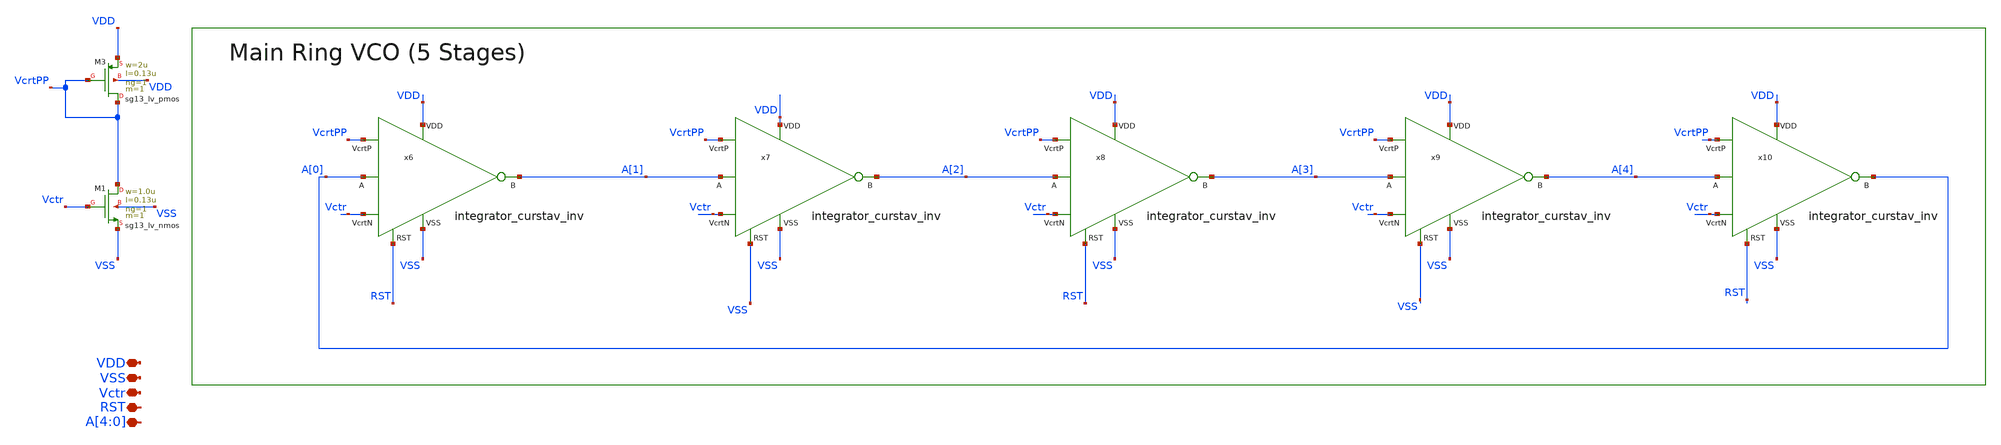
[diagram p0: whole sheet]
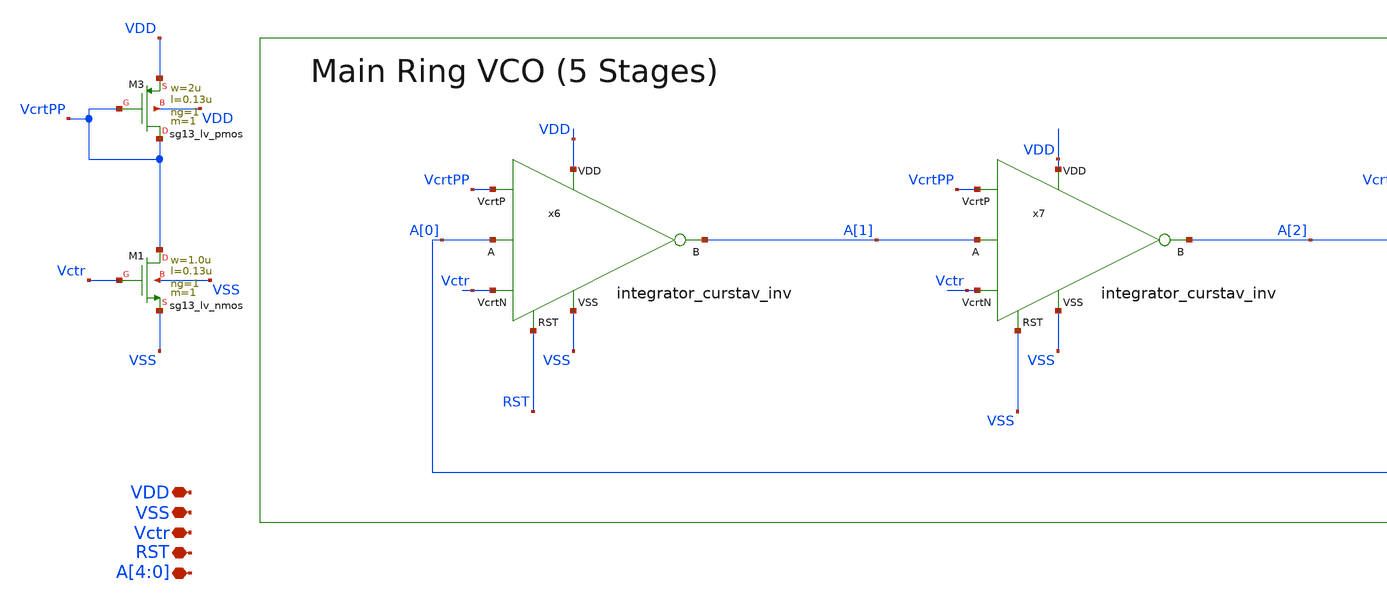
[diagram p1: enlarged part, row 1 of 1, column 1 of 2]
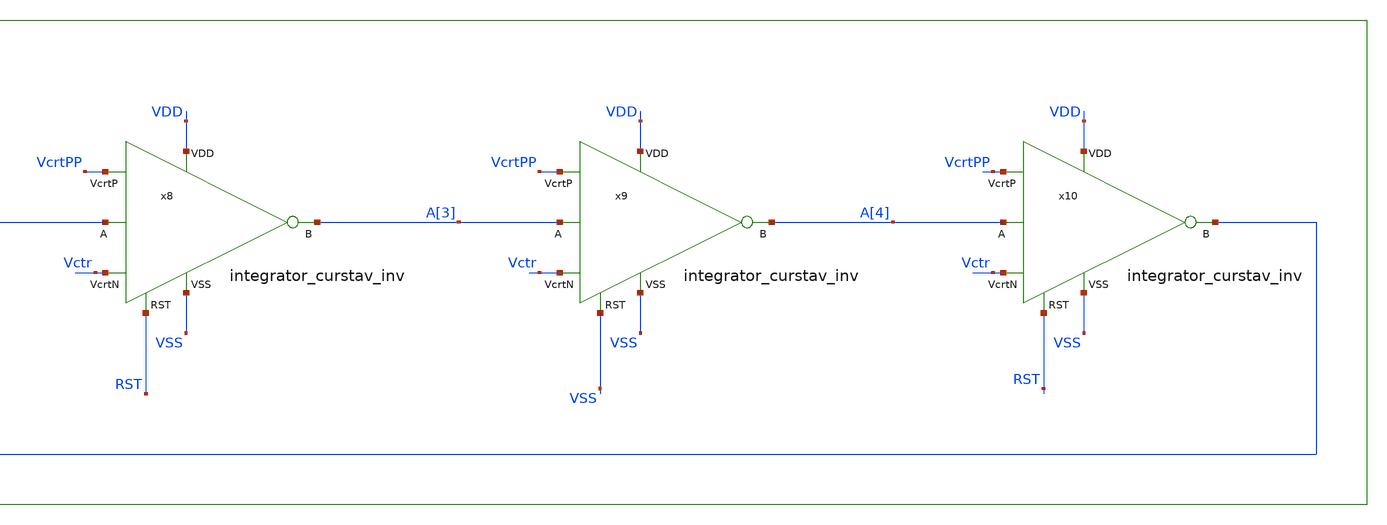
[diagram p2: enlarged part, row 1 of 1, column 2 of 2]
** sch_path: work/integrator_ring-oscillator/xschem/integrator_ring_oscillator.sch
**.subckt integrator_ring_oscillator VDD Vctr VSS RST A[4],A[3],A[2],A[1],A[0]
*.iopin VDD
*.iopin Vctr
*.iopin VSS
*.iopin RST
*.iopin A[4],A[3],A[2],A[1],A[0]
x6 VDD VcrtPP A[0] A[1] Vctr VSS RST integrator_curstav_inv
x7 VDD VcrtPP A[1] A[2] Vctr VSS VSS integrator_curstav_inv
x8 VDD VcrtPP A[2] A[3] Vctr VSS RST integrator_curstav_inv
x9 VDD VcrtPP A[3] A[4] Vctr VSS VSS integrator_curstav_inv
x10 VDD VcrtPP A[4] A[0] Vctr VSS RST integrator_curstav_inv
XM1 VcrtPP Vctr VSS VSS sg13_lv_nmos w=1.0u l=0.13u ng=1 m=1 mm_ok=1
XM3 VcrtPP VcrtPP VDD VDD sg13_lv_pmos w=2u l=0.13u ng=1 m=1 mm_ok=1
**.ends
.end
